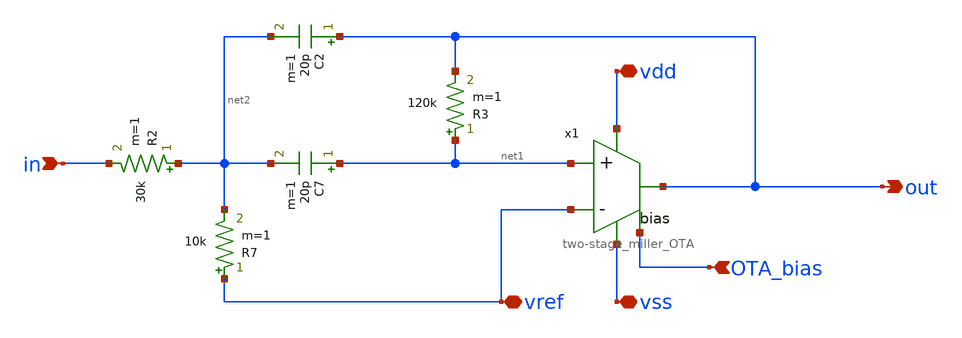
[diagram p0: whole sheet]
** sch_path: design/analog/BPF/BPF.sch
**.subckt BPF out in vdd vss vref OTA_bias
*.opin out
*.ipin in
*.iopin vdd
*.iopin vss
*.iopin vref
*.ipin OTA_bias
R2 net2 in 30k m=1
C2 out net2 20p m=1
R3 net1 out 120k m=1
R7 vref net2 10k m=1
C7 net1 net2 20p m=1
x1 vdd out net1 vref OTA_bias vss two-stage_miller_OTA
**.ends

* expanding   symbol:  acoustic_ranger_2026/two-stage_miller_OTA.sym # of pins=6
** sym_path: design/analog/OTA/two-stage_miller_OTA.sym
** sch_path: design/analog/OTA/two-stage_miller_OTA.sch
.subckt two-stage_miller_OTA vdd out in+ in- bias vss
*.ipin in-
*.ipin in+
*.opin out
*.iopin vdd
*.iopin vss
*.ipin bias
XM1 net2 in+ net1 vdd pfet_03v3 L=1u W=49.6u nf=1 ad='int((nf+1)/2) * W/nf * 0.18u' as='int((nf+2)/2) * W/nf * 0.18u'
+ pd='2*int((nf+1)/2) * (W/nf + 0.18u)' ps='2*int((nf+2)/2) * (W/nf + 0.18u)' nrd='0.18u / W' nrs='0.18u / W'
+ sa=0 sb=0 sd=0 m=1
XM2 net3 in- net1 vdd pfet_03v3 L=1u W=49.6u nf=1 ad='int((nf+1)/2) * W/nf * 0.18u' as='int((nf+2)/2) * W/nf * 0.18u'
+ pd='2*int((nf+1)/2) * (W/nf + 0.18u)' ps='2*int((nf+2)/2) * (W/nf + 0.18u)' nrd='0.18u / W' nrs='0.18u / W'
+ sa=0 sb=0 sd=0 m=1
XM14 net3 net2 vss vss nfet_03v3 L=3u W=15.4u nf=1 ad='int((nf+1)/2) * W/nf * 0.18u' as='int((nf+2)/2) * W/nf * 0.18u'
+ pd='2*int((nf+1)/2) * (W/nf + 0.18u)' ps='2*int((nf+2)/2) * (W/nf + 0.18u)' nrd='0.18u / W' nrs='0.18u / W'
+ sa=0 sb=0 sd=0 m=1
XM15 net2 net2 vss vss nfet_03v3 L=3u W=15.4u nf=1 ad='int((nf+1)/2) * W/nf * 0.18u' as='int((nf+2)/2) * W/nf * 0.18u'
+ pd='2*int((nf+1)/2) * (W/nf + 0.18u)' ps='2*int((nf+2)/2) * (W/nf + 0.18u)' nrd='0.18u / W' nrs='0.18u / W'
+ sa=0 sb=0 sd=0 m=1
XM3 out net3 vss vss nfet_03v3 L=500n W=15.4u nf=1 ad='int((nf+1)/2) * W/nf * 0.18u' as='int((nf+2)/2) * W/nf * 0.18u'
+ pd='2*int((nf+1)/2) * (W/nf + 0.18u)' ps='2*int((nf+2)/2) * (W/nf + 0.18u)' nrd='0.18u / W' nrs='0.18u / W'
+ sa=0 sb=0 sd=0 m=1
C1 out net3 150f m=1
XM4 net1 bias vdd vdd pfet_03v3 L=30u W=63.9u nf=1 ad='int((nf+1)/2) * W/nf * 0.18u' as='int((nf+2)/2) * W/nf * 0.18u'
+ pd='2*int((nf+1)/2) * (W/nf + 0.18u)' ps='2*int((nf+2)/2) * (W/nf + 0.18u)' nrd='0.18u / W' nrs='0.18u / W'
+ sa=0 sb=0 sd=0 m=6
XM5 out bias vdd vdd pfet_03v3 L=30u W=55.75u nf=1 ad='int((nf+1)/2) * W/nf * 0.18u' as='int((nf+2)/2) * W/nf * 0.18u'
+ pd='2*int((nf+1)/2) * (W/nf + 0.18u)' ps='2*int((nf+2)/2) * (W/nf + 0.18u)' nrd='0.18u / W' nrs='0.18u / W'
+ sa=0 sb=0 sd=0 m=15
.ends

.end
